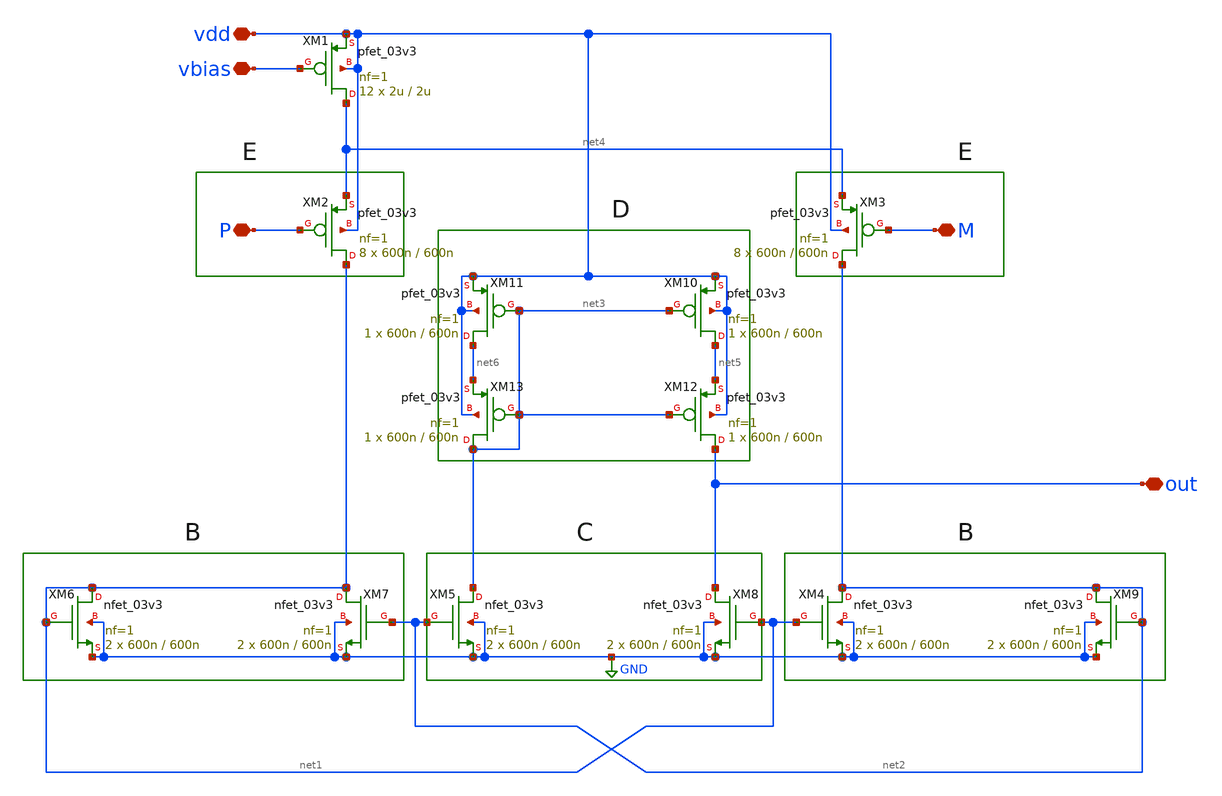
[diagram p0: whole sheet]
** sch_path: Clock_Reference/symbols_clock/comparatornew.sch
**.subckt comparatornew out M P vbias vdd
*.iopin out
*.iopin M
*.iopin P
*.iopin vbias
*.iopin vdd
XM1 net4 vbias vdd vdd pfet_03v3 L=2u W=2u nf=1 ad='int((nf+1)/2) * W/nf * 0.18u' as='int((nf+2)/2) * W/nf * 0.18u'
+ pd='2*int((nf+1)/2) * (W/nf + 0.18u)' ps='2*int((nf+2)/2) * (W/nf + 0.18u)' nrd='0.18u / W' nrs='0.18u / W'
+ sa=0 sb=0 sd=0 m=12
XM2 net1 P net4 vdd pfet_03v3 L=600n W=600n nf=1 ad='int((nf+1)/2) * W/nf * 0.18u' as='int((nf+2)/2) * W/nf * 0.18u'
+ pd='2*int((nf+1)/2) * (W/nf + 0.18u)' ps='2*int((nf+2)/2) * (W/nf + 0.18u)' nrd='0.18u / W' nrs='0.18u / W'
+ sa=0 sb=0 sd=0 m=8
XM3 net2 M net4 vdd pfet_03v3 L=600n W=600n nf=1 ad='int((nf+1)/2) * W/nf * 0.18u' as='int((nf+2)/2) * W/nf * 0.18u'
+ pd='2*int((nf+1)/2) * (W/nf + 0.18u)' ps='2*int((nf+2)/2) * (W/nf + 0.18u)' nrd='0.18u / W' nrs='0.18u / W'
+ sa=0 sb=0 sd=0 m=8
XM4 net2 net1 GND GND nfet_03v3 L=600n W=600n nf=1 ad='int((nf+1)/2) * W/nf * 0.18u' as='int((nf+2)/2) * W/nf * 0.18u'
+ pd='2*int((nf+1)/2) * (W/nf + 0.18u)' ps='2*int((nf+2)/2) * (W/nf + 0.18u)' nrd='0.18u / W' nrs='0.18u / W'
+ sa=0 sb=0 sd=0 m=2
XM5 net3 net2 GND GND nfet_03v3 L=600n W=600n nf=1 ad='int((nf+1)/2) * W/nf * 0.18u' as='int((nf+2)/2) * W/nf * 0.18u'
+ pd='2*int((nf+1)/2) * (W/nf + 0.18u)' ps='2*int((nf+2)/2) * (W/nf + 0.18u)' nrd='0.18u / W' nrs='0.18u / W'
+ sa=0 sb=0 sd=0 m=2
XM6 net1 net1 GND GND nfet_03v3 L=600n W=600n nf=1 ad='int((nf+1)/2) * W/nf * 0.18u' as='int((nf+2)/2) * W/nf * 0.18u'
+ pd='2*int((nf+1)/2) * (W/nf + 0.18u)' ps='2*int((nf+2)/2) * (W/nf + 0.18u)' nrd='0.18u / W' nrs='0.18u / W'
+ sa=0 sb=0 sd=0 m=2
XM7 net1 net2 GND GND nfet_03v3 L=600n W=600n nf=1 ad='int((nf+1)/2) * W/nf * 0.18u' as='int((nf+2)/2) * W/nf * 0.18u'
+ pd='2*int((nf+1)/2) * (W/nf + 0.18u)' ps='2*int((nf+2)/2) * (W/nf + 0.18u)' nrd='0.18u / W' nrs='0.18u / W'
+ sa=0 sb=0 sd=0 m=2
XM8 out net1 GND GND nfet_03v3 L=600n W=600n nf=1 ad='int((nf+1)/2) * W/nf * 0.18u' as='int((nf+2)/2) * W/nf * 0.18u'
+ pd='2*int((nf+1)/2) * (W/nf + 0.18u)' ps='2*int((nf+2)/2) * (W/nf + 0.18u)' nrd='0.18u / W' nrs='0.18u / W'
+ sa=0 sb=0 sd=0 m=2
XM9 net2 net2 GND GND nfet_03v3 L=600n W=600n nf=1 ad='int((nf+1)/2) * W/nf * 0.18u' as='int((nf+2)/2) * W/nf * 0.18u'
+ pd='2*int((nf+1)/2) * (W/nf + 0.18u)' ps='2*int((nf+2)/2) * (W/nf + 0.18u)' nrd='0.18u / W' nrs='0.18u / W'
+ sa=0 sb=0 sd=0 m=2
XM10 net5 net3 vdd vdd pfet_03v3 L=600n W=600n nf=1 ad='int((nf+1)/2) * W/nf * 0.18u' as='int((nf+2)/2) * W/nf * 0.18u'
+ pd='2*int((nf+1)/2) * (W/nf + 0.18u)' ps='2*int((nf+2)/2) * (W/nf + 0.18u)' nrd='0.18u / W' nrs='0.18u / W'
+ sa=0 sb=0 sd=0 m=1
XM11 net6 net3 vdd vdd pfet_03v3 L=600n W=600n nf=1 ad='int((nf+1)/2) * W/nf * 0.18u' as='int((nf+2)/2) * W/nf * 0.18u'
+ pd='2*int((nf+1)/2) * (W/nf + 0.18u)' ps='2*int((nf+2)/2) * (W/nf + 0.18u)' nrd='0.18u / W' nrs='0.18u / W'
+ sa=0 sb=0 sd=0 m=1
XM12 out net3 net5 vdd pfet_03v3 L=600n W=600n nf=1 ad='int((nf+1)/2) * W/nf * 0.18u' as='int((nf+2)/2) * W/nf * 0.18u'
+ pd='2*int((nf+1)/2) * (W/nf + 0.18u)' ps='2*int((nf+2)/2) * (W/nf + 0.18u)' nrd='0.18u / W' nrs='0.18u / W'
+ sa=0 sb=0 sd=0 m=1
XM13 net3 net3 net6 vdd pfet_03v3 L=600n W=600n nf=1 ad='int((nf+1)/2) * W/nf * 0.18u' as='int((nf+2)/2) * W/nf * 0.18u'
+ pd='2*int((nf+1)/2) * (W/nf + 0.18u)' ps='2*int((nf+2)/2) * (W/nf + 0.18u)' nrd='0.18u / W' nrs='0.18u / W'
+ sa=0 sb=0 sd=0 m=1
**.ends
.GLOBAL GND
.end
